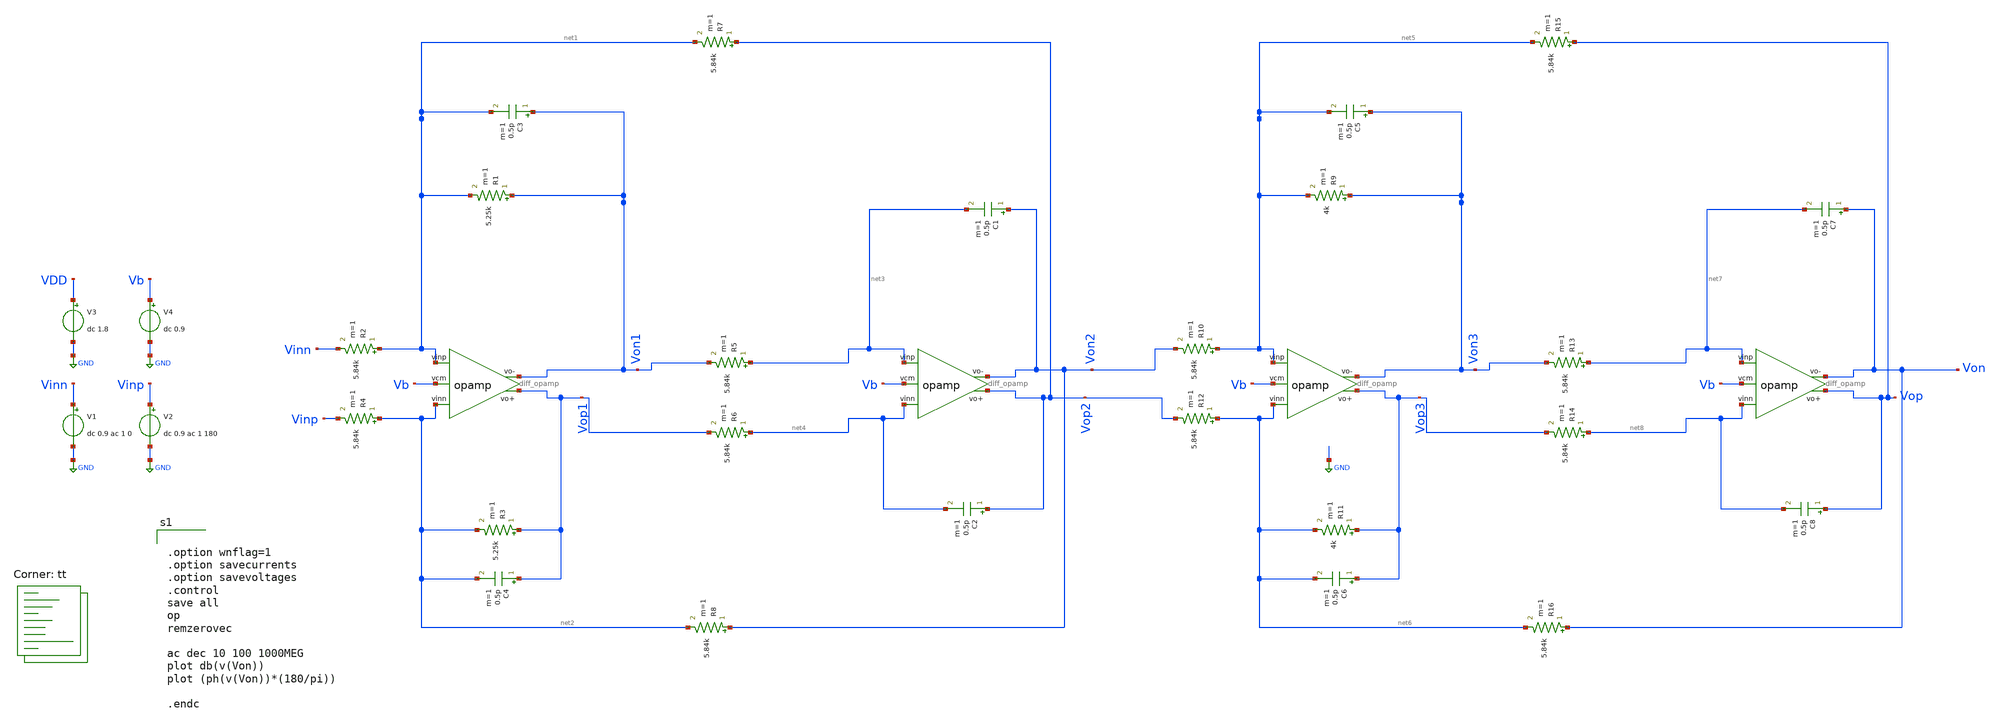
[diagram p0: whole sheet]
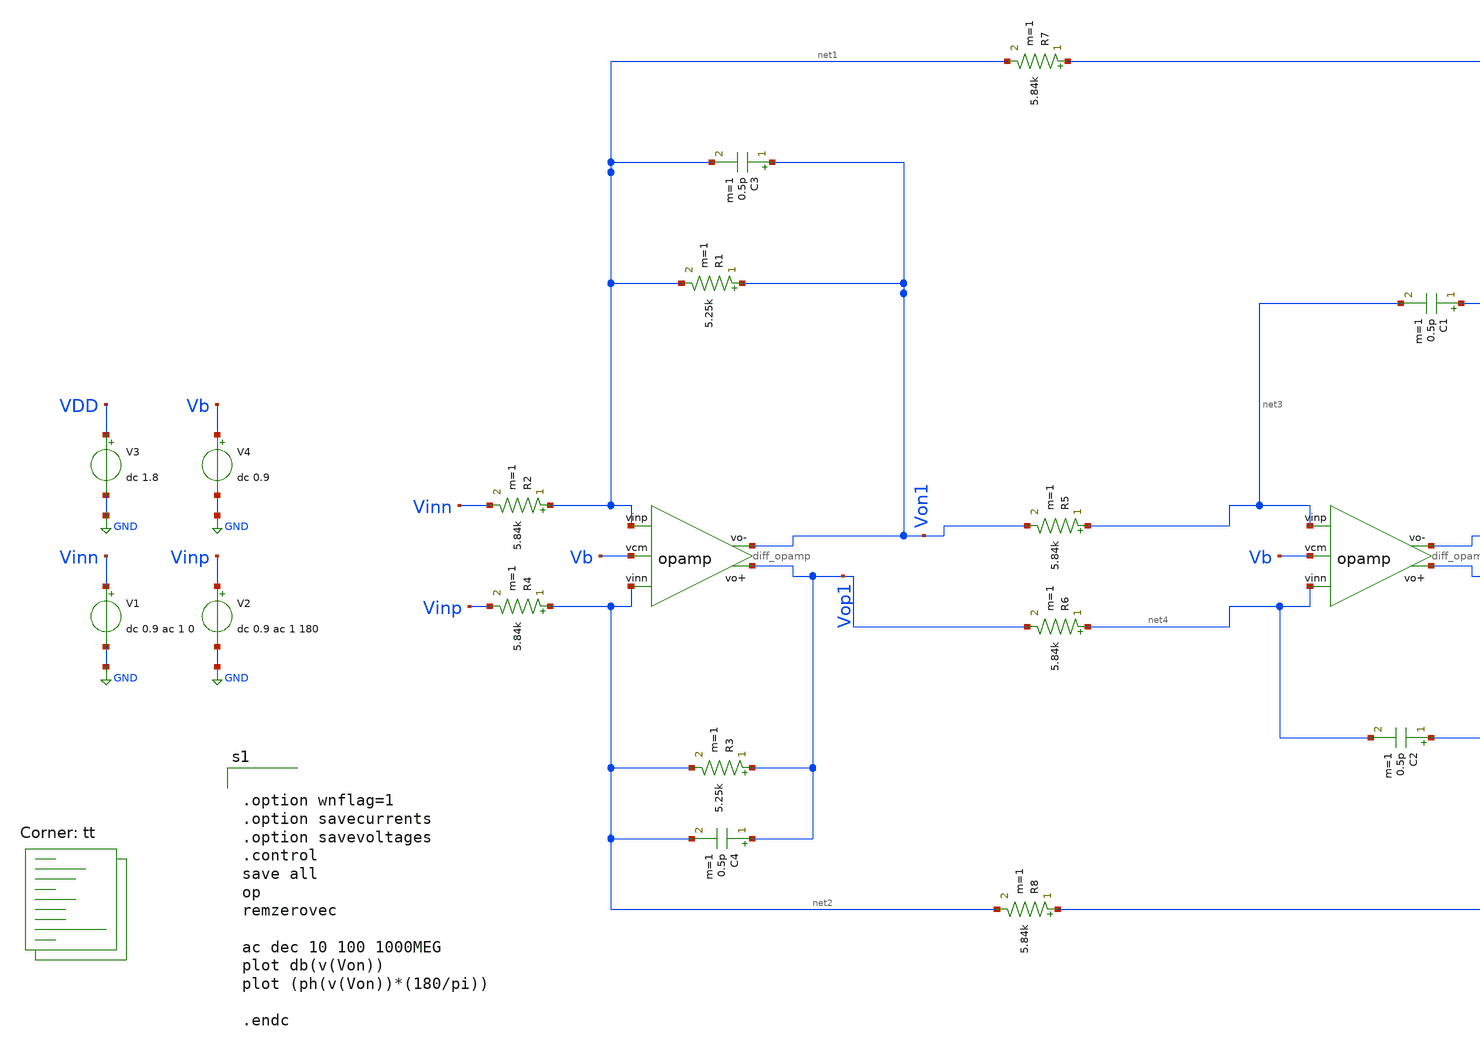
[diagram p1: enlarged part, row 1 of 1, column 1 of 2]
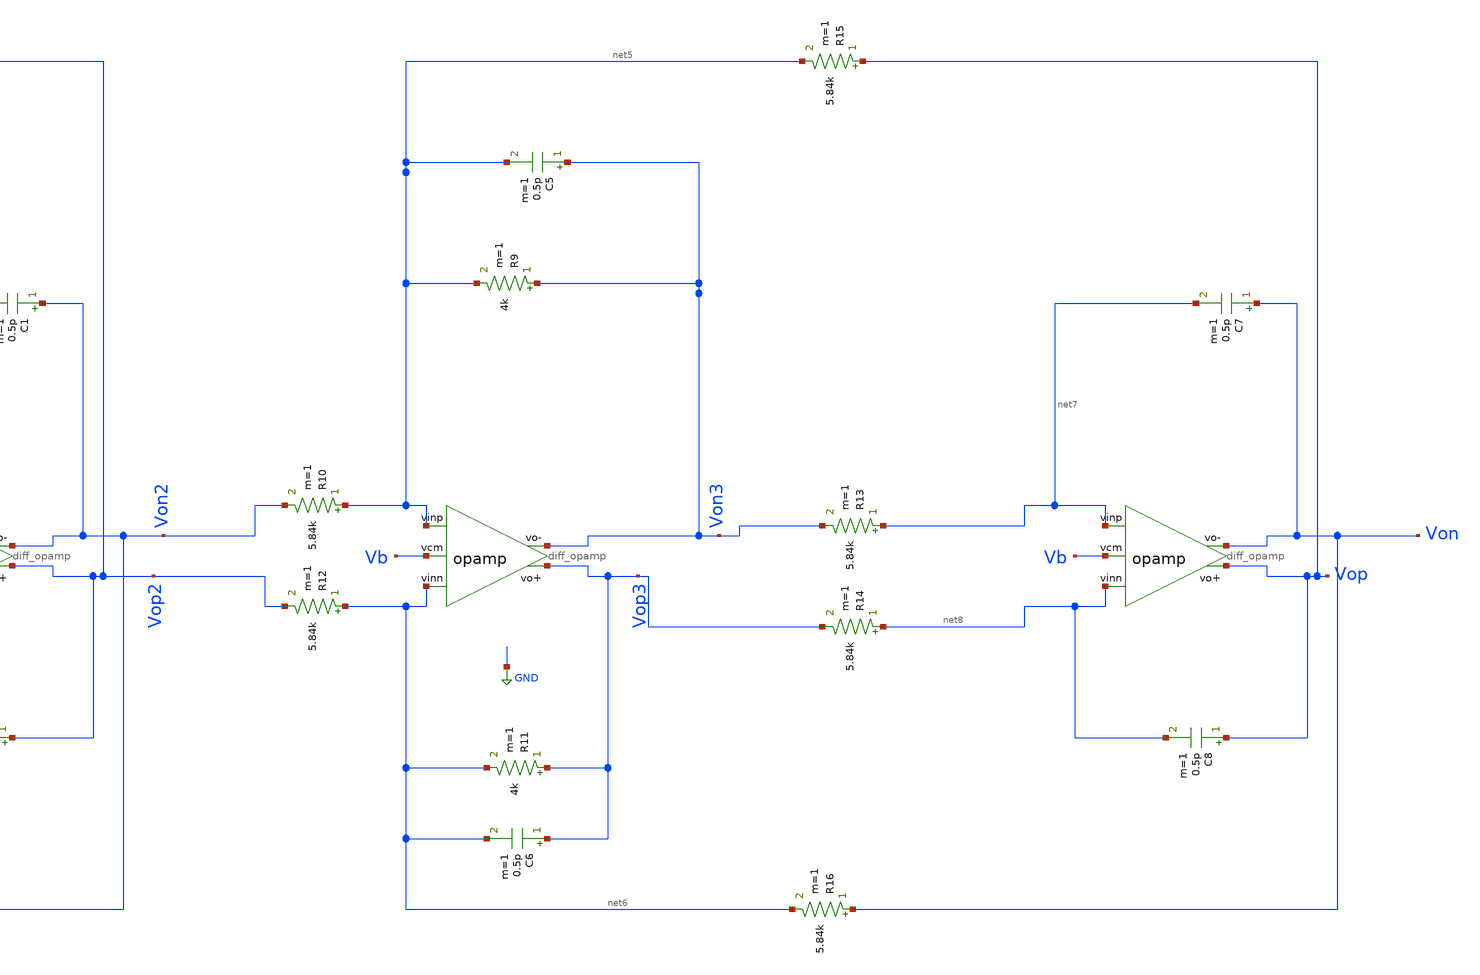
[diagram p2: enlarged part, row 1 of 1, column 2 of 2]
** sch_path: Simulation files/Filter_using_ideal_opamp.sch
**.subckt Filter_using_ideal_opamp
V1 Vinn GND dc 0.9 ac 1 0
V2 Vinp GND dc 0.9 ac 1 180
V3 VDD GND dc 1.8
V4 Vb GND dc 0.9
R1 Von1 net1 5.25k m=1
R2 net1 Vinn 5.84k m=1
R3 Vop1 net2 5.25k m=1
R4 net2 Vinp 5.84k m=1
C3 Von1 net1 0.5p m=1
C4 Vop1 net2 0.5p m=1
R5 net3 Von1 5.84k m=1
R6 net4 Vop1 5.84k m=1
C1 Von2 net3 0.5p m=1
C2 Vop2 net4 0.5p m=1
R7 Vop2 net1 5.84k m=1
R8 Von2 net2 5.84k m=1
R9 Von3 net5 4k m=1
R10 net5 Von2 5.84k m=1
R11 Vop3 net6 4k m=1
R12 net6 Vop2 5.84k m=1
C5 Von3 net5 0.5p m=1
C6 Vop3 net6 0.5p m=1
R13 net7 Von3 5.84k m=1
R14 net8 Vop3 5.84k m=1
C7 Von net7 0.5p m=1
C8 Vop net8 0.5p m=1
R15 Vop net5 5.84k m=1
R16 Von net6 5.84k m=1
x1 Von1 Vb net1 net2 Vop1 diff_opamp
x2 Von2 Vb net3 net4 Vop2 diff_opamp
x3 Von3 Vb net5 net6 Vop3 diff_opamp
x4 Von Vb net7 net8 Vop diff_opamp
**** begin user architecture code
.lib $::SKYWATER_MODELS/sky130.lib.spice tt


.option wnflag=1
.option savecurrents
.option savevoltages
.control
save all
op
remzerovec

ac dec 10 100 1000MEG
plot db(v(Von))
plot (ph(v(Von))*(180/pi))

.endc


**** end user architecture code
**.ends
.GLOBAL GND
.end
